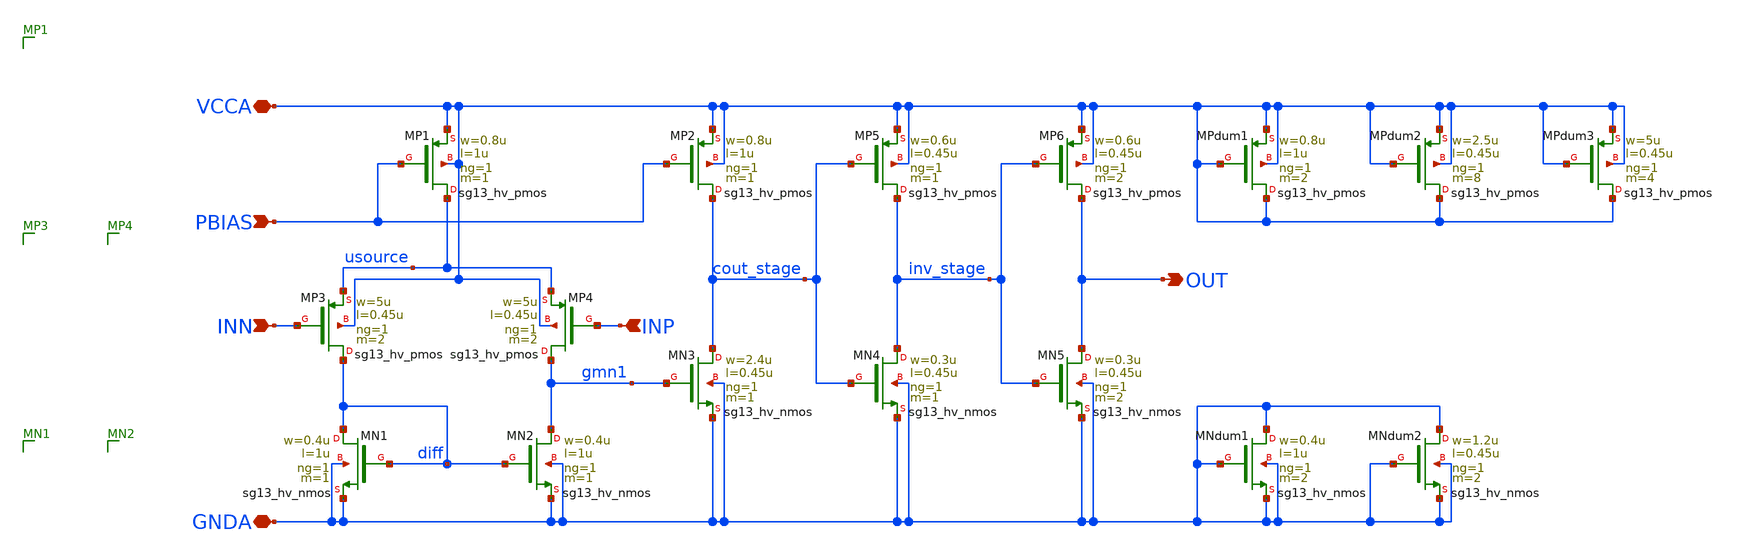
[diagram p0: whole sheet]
** sch_path: macros/heichips26_FAIf/macros/comparator/schematic/xschem/555_comparator.sch
**.subckt 555_comparator INP VCCA OUT GNDA INN PBIAS
*.ipin INP
*.iopin VCCA
*.opin OUT
*.iopin GNDA
*.ipin INN
*.ipin PBIAS
XMP1 usource PBIAS VCCA VCCA sg13_hv_pmos w=0.8u l=1u ng=1 m=1 mm_ok=1
XMN1 diff diff GNDA GNDA sg13_hv_nmos w=0.4u l=1u ng=1 m=1 mm_ok=1
XMN2 gmn1 diff GNDA GNDA sg13_hv_nmos w=0.4u l=1u ng=1 m=1 mm_ok=1
XMP4 gmn1 INP usource VCCA sg13_hv_pmos w=5u l=0.45u ng=1 m=2 mm_ok=1
XMP3 diff INN usource VCCA sg13_hv_pmos w=5u l=0.45u ng=1 m=2 mm_ok=1
XMP2 cout_stage PBIAS VCCA VCCA sg13_hv_pmos w=0.8u l=1u ng=1 m=1 mm_ok=1
XMN3 cout_stage gmn1 GNDA GNDA sg13_hv_nmos w=2.4u l=0.45u ng=1 m=1 mm_ok=1
XMN4 inv_stage cout_stage GNDA GNDA sg13_hv_nmos w=0.3u l=0.45u ng=1 m=1 mm_ok=1
XMP5 inv_stage cout_stage VCCA VCCA sg13_hv_pmos w=0.6u l=0.45u ng=1 m=1 mm_ok=1
XMN5 OUT inv_stage GNDA GNDA sg13_hv_nmos w=0.3u l=0.45u ng=1 m=2 mm_ok=1
XMP6 OUT inv_stage VCCA VCCA sg13_hv_pmos w=0.6u l=0.45u ng=1 m=2 mm_ok=1
XMPdum1 VCCA VCCA VCCA VCCA sg13_hv_pmos w=0.8u l=1u ng=1 m=2 mm_ok=1
XMPdum2 VCCA VCCA VCCA VCCA sg13_hv_pmos w=2.5u l=0.45u ng=1 m=8 mm_ok=1
XMPdum3 VCCA VCCA VCCA VCCA sg13_hv_pmos w=5u l=0.45u ng=1 m=4 mm_ok=1
XMNdum2 GNDA GNDA GNDA GNDA sg13_hv_nmos w=1.2u l=0.45u ng=1 m=2 mm_ok=1
XMNdum1 GNDA GNDA GNDA GNDA sg13_hv_nmos w=0.4u l=1u ng=1 m=2 mm_ok=1
**.ends
.end
